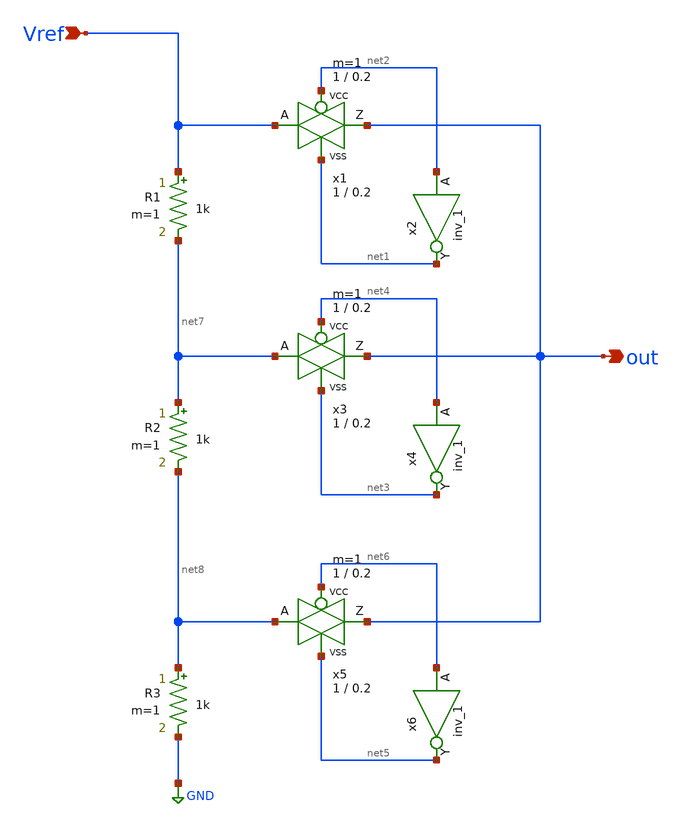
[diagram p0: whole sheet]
** sch_path: voltageselector.sch
**.subckt voltageselector Vref out
*.ipin Vref
*.opin out
x1 out Vref net2 net1 VCC VSS passgate W_N=1 L_N=0.2 W_P=1 L_P=0.2 m=1
R1 Vref net7 1k m=1
R2 net7 net8 1k m=1
R3 net8 GND 1k m=1
x2 net2 VGND VNB VPB VPWR net1 sky130_fd_sc_hd__inv_1
x3 out net7 net4 net3 VCC VSS passgate W_N=1 L_N=0.2 W_P=1 L_P=0.2 m=1
x4 net4 VGND VNB VPB VPWR net3 sky130_fd_sc_hd__inv_1
x5 out net8 net6 net5 VCC VSS passgate W_N=1 L_N=0.2 W_P=1 L_P=0.2 m=1
x6 net6 VGND VNB VPB VPWR net5 sky130_fd_sc_hd__inv_1
**.ends

* expanding   symbol:  xschem_sky130/sky130_tests/passgate.sym # of pins=4
** sym_path: xschem_sky130/sky130_tests/passgate.sym
** sch_path: xschem_sky130/sky130_tests/passgate.sch
.subckt passgate Z A GP GN VCCBPIN VSSBPIN  W_N=1 L_N=0.2 W_P=1 L_P=0.2

*.iopin A
*.iopin Z
*.ipin GP
*.ipin GN
XM1 A GN Z VSS sky130_fd_pr__nfet_01v8 W=W_N L=L_N ad='W * 0.29' pd='W + 2 * 0.29' as='W * 0.29' ps='W + 2 * 0.29'
+ nrd=0 nrs=0 sa=0 sb=0 sd=0 nf=1 mult=1
XM2 A GP Z VCC sky130_fd_pr__pfet_01v8 W=W_P L=L_P ad='W * 0.29' pd='W + 2 * 0.29' as='W * 0.29' ps='W + 2 * 0.29'
+ nrd=0 nrs=0 sa=0 sb=0 sd=0 nf=1 mult=1
.ends

.GLOBAL GND
.end
